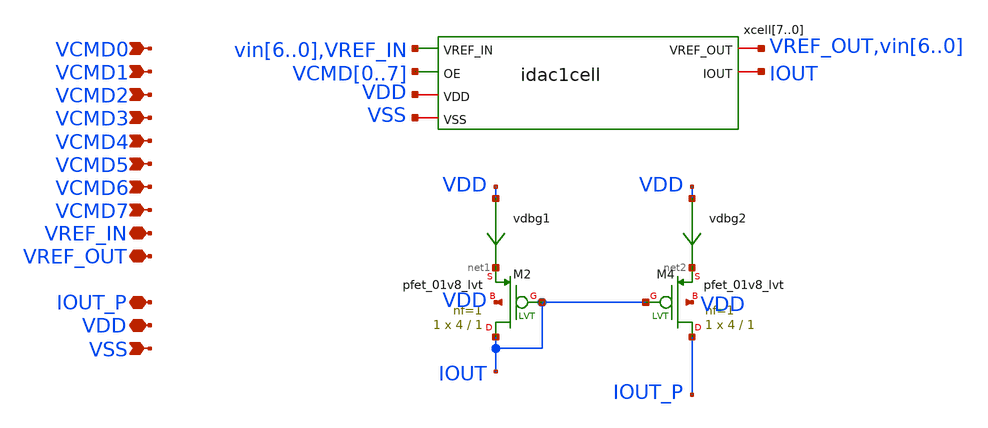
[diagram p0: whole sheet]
** sch_path: tt_um_emilian_rf_playground/xschem/idac1.sch
**.subckt idac1 VSS VREF_IN VDD VCMD7 VCMD6 VCMD5 VCMD4 VCMD3 VCMD2 VCMD1 VCMD0 VREF_OUT IOUT_P
*.ipin VSS
*.iopin VREF_IN
*.iopin VDD
*.ipin VCMD7
*.ipin VCMD6
*.ipin VCMD5
*.ipin VCMD4
*.ipin VCMD3
*.ipin VCMD2
*.ipin VCMD1
*.ipin VCMD0
*.iopin VREF_OUT
*.iopin IOUT_P
xcell7 vin6 VREF_OUT IOUT VDD VSS VCMD0 idac1cell
xcell6 vin5 vin6 IOUT VDD VSS VCMD1 idac1cell
xcell5 vin4 vin5 IOUT VDD VSS VCMD2 idac1cell
xcell4 vin3 vin4 IOUT VDD VSS VCMD3 idac1cell
xcell3 vin2 vin3 IOUT VDD VSS VCMD4 idac1cell
xcell2 vin1 vin2 IOUT VDD VSS VCMD5 idac1cell
xcell1 vin0 vin1 IOUT VDD VSS VCMD6 idac1cell
xcell0 VREF_IN vin0 IOUT VDD VSS VCMD7 idac1cell
XM2 IOUT IOUT net1 VDD sky130_fd_pr__pfet_01v8_lvt L=1 W=4 nf=1 ad='int((nf+1)/2) * W/nf * 0.29' as='int((nf+2)/2) * W/nf * 0.29'
+ pd='2*int((nf+1)/2) * (W/nf + 0.29)' ps='2*int((nf+2)/2) * (W/nf + 0.29)' nrd='0.29 / W' nrs='0.29 / W'
+ sa=0 sb=0 sd=0 mult=1 m=1
vdbg1 VDD net1 0
.save i(vdbg1)
XM4 IOUT_P IOUT net2 VDD sky130_fd_pr__pfet_01v8_lvt L=1 W=4 nf=1 ad='int((nf+1)/2) * W/nf * 0.29' as='int((nf+2)/2) * W/nf * 0.29'
+ pd='2*int((nf+1)/2) * (W/nf + 0.29)' ps='2*int((nf+2)/2) * (W/nf + 0.29)' nrd='0.29 / W' nrs='0.29 / W'
+ sa=0 sb=0 sd=0 mult=1 m=1
vdbg2 VDD net2 0
.save i(vdbg2)
**.ends

* expanding   symbol:  idac1cell.sym # of pins=6
** sym_path: tt_um_emilian_rf_playground/xschem/idac1cell.sym
** sch_path: tt_um_emilian_rf_playground/xschem/idac1cell.sch
.subckt idac1cell VREF_IN VREF_OUT IOUT VDD VSS OE
*.ipin VSS
*.iopin VREF_OUT
*.ipin VREF_IN
*.iopin VDD
*.iopin IOUT
*.ipin OE
XM3 net1 net1 net2 net2 sky130_fd_pr__nfet_01v8_lvt L=1 W=2 nf=1 ad='int((nf+1)/2) * W/nf * 0.29' as='int((nf+2)/2) * W/nf * 0.29'
+ pd='2*int((nf+1)/2) * (W/nf + 0.29)' ps='2*int((nf+2)/2) * (W/nf + 0.29)' nrd='0.29 / W' nrs='0.29 / W'
+ sa=0 sb=0 sd=0 mult=1 m=1
XM4 net1 net1 VSS VSS sky130_fd_pr__nfet_01v8_lvt L=1 W=2 nf=1 ad='int((nf+1)/2) * W/nf * 0.29' as='int((nf+2)/2) * W/nf * 0.29'
+ pd='2*int((nf+1)/2) * (W/nf + 0.29)' ps='2*int((nf+2)/2) * (W/nf + 0.29)' nrd='0.29 / W' nrs='0.29 / W'
+ sa=0 sb=0 sd=0 mult=1 m=1
XM1 net1 VREF_IN VDD VDD sky130_fd_pr__pfet_01v8_lvt L=1 W=4 nf=1 ad='int((nf+1)/2) * W/nf * 0.29' as='int((nf+2)/2) * W/nf * 0.29'
+ pd='2*int((nf+1)/2) * (W/nf + 0.29)' ps='2*int((nf+2)/2) * (W/nf + 0.29)' nrd='0.29 / W' nrs='0.29 / W'
+ sa=0 sb=0 sd=0 mult=1 m=1
XM5 net3 net1 VSS VSS sky130_fd_pr__nfet_01v8_lvt L=1 W=2 nf=1 ad='int((nf+1)/2) * W/nf * 0.29' as='int((nf+2)/2) * W/nf * 0.29'
+ pd='2*int((nf+1)/2) * (W/nf + 0.29)' ps='2*int((nf+2)/2) * (W/nf + 0.29)' nrd='0.29 / W' nrs='0.29 / W'
+ sa=0 sb=0 sd=0 mult=1 m=1
XM2 VREF_OUT VREF_OUT VDD VDD sky130_fd_pr__pfet_01v8_lvt L=1 W=4 nf=1 ad='int((nf+1)/2) * W/nf * 0.29'
+ as='int((nf+2)/2) * W/nf * 0.29' pd='2*int((nf+1)/2) * (W/nf + 0.29)' ps='2*int((nf+2)/2) * (W/nf + 0.29)'
+ nrd='0.29 / W' nrs='0.29 / W' sa=0 sb=0 sd=0 mult=1 m=1
XM6 vdrain2 net1 VSS VSS sky130_fd_pr__nfet_01v8_lvt L=1 W=2 nf=1 ad='int((nf+1)/2) * W/nf * 0.29' as='int((nf+2)/2) * W/nf * 0.29'
+ pd='2*int((nf+1)/2) * (W/nf + 0.29)' ps='2*int((nf+2)/2) * (W/nf + 0.29)' nrd='0.29 / W' nrs='0.29 / W'
+ sa=0 sb=0 sd=0 mult=1 m=1
XM7 net4 OE vdrain2 VSS sky130_fd_pr__nfet_01v8_lvt L=1 W=2 nf=1 ad='int((nf+1)/2) * W/nf * 0.29' as='int((nf+2)/2) * W/nf * 0.29'
+ pd='2*int((nf+1)/2) * (W/nf + 0.29)' ps='2*int((nf+2)/2) * (W/nf + 0.29)' nrd='0.29 / W' nrs='0.29 / W'
+ sa=0 sb=0 sd=0 mult=1 m=1
vmeas VREF_OUT net3 0
.save i(vmeas)
viout IOUT net4 0
.save i(viout)
vref net2 VSS 0
.save i(vref)
.ends

.end
